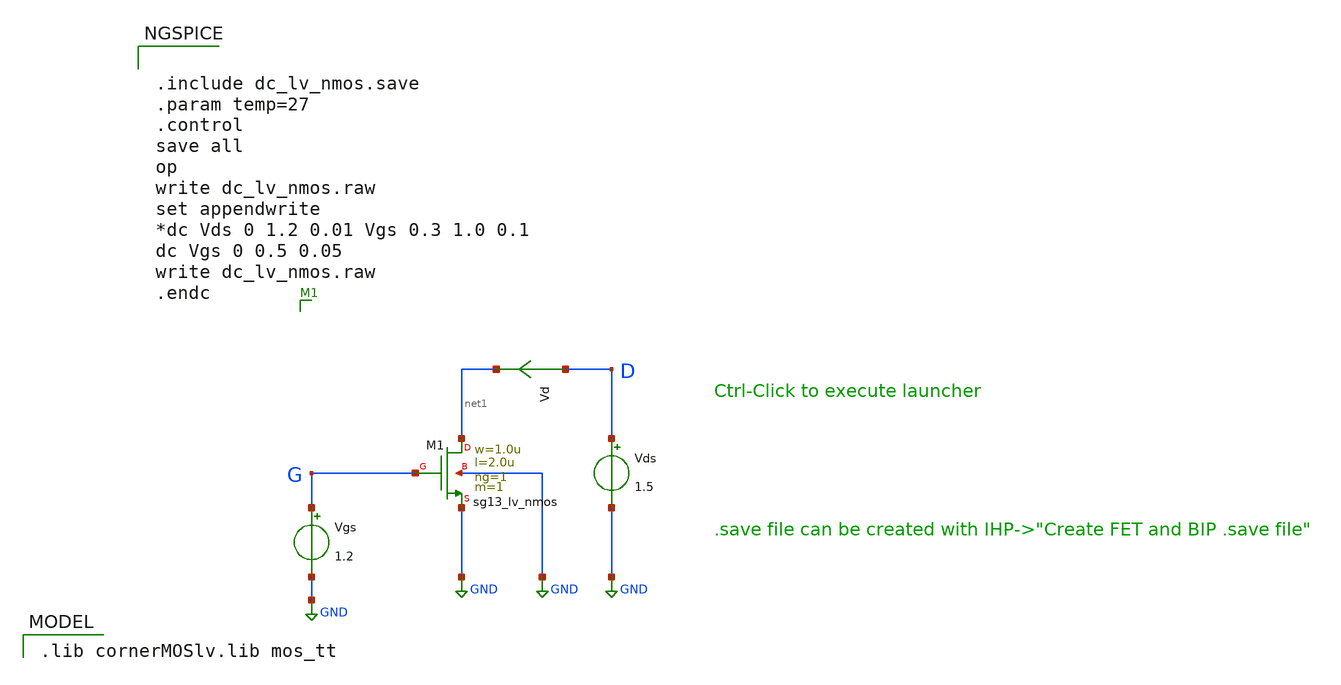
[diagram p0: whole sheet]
** sch_path: blocks/composite/dpi_adexp_neuron/design_data/xschem/dc_lv_nmos.sch
* Copyright 2023 IHP PDK Authors
**.subckt dc_lv_nmos
Vgs G GND 1.2
Vds D GND 1.5
Vd D net1 0
.save i(vd)
XM1 net1 G GND GND sg13_lv_nmos w=1.0u l=2.0u ng=1 m=1 mm_ok=1
**** begin user architecture code
 .lib cornerMOSlv.lib mos_tt



.include dc_lv_nmos.save
.param temp=27
.control
save all
op
write dc_lv_nmos.raw
set appendwrite
*dc Vds 0 1.2 0.01 Vgs 0.3 1.0 0.1
dc Vgs 0 0.5 0.05
write dc_lv_nmos.raw
.endc


**** end user architecture code
**.ends
.GLOBAL GND
.end
